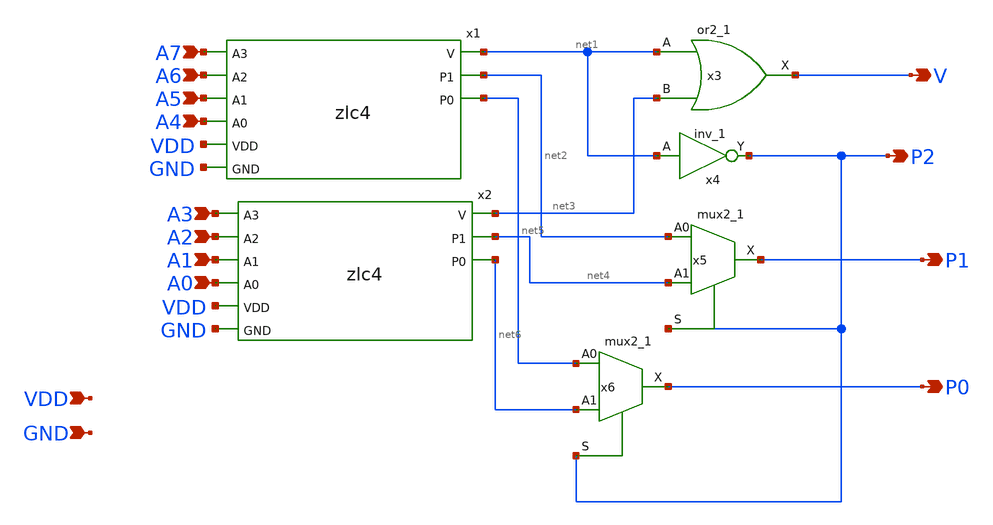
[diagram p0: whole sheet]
** sch_path: xschem/zlc8.sch
**.subckt zlc8 A7 A6 A5 A4 A3 A2 A1 A0 V P2 P1 P0 VDD GND
*.ipin A7
*.ipin A6
*.ipin A5
*.ipin A4
*.ipin A3
*.ipin A2
*.ipin A1
*.ipin A0
*.opin V
*.opin P2
*.opin P1
*.opin P0
*.ipin VDD
*.ipin GND
x3 net1 net3 GND GND VDD VDD V sky130_fd_sc_hd__or2_1
x4 net1 GND GND VDD VDD P2 sky130_fd_sc_hd__inv_1
x5 net2 net4 P2 GND GND VDD VDD P1 sky130_fd_sc_hd__mux2_1
x6 net5 net6 P2 GND GND VDD VDD P0 sky130_fd_sc_hd__mux2_1
x1 A7 net1 A6 net2 A5 A4 net5 VDD GND zlc4
x2 A3 net3 A2 net4 A1 A0 net6 VDD GND zlc4
**.ends

* expanding   symbol:  zlc4.sym # of pins=9
** sym_path: xschem/zlc4.sym
** sch_path: xschem/zlc4.sch
.subckt zlc4 A3 V A2 P1 A1 A0 P0 VDD GND
*.ipin A3
*.ipin A2
*.ipin A1
*.ipin A0
*.opin V
*.opin P1
*.opin P0
*.ipin VDD
*.ipin GND
x3 net1 net2 GND GND VDD VDD V sky130_fd_sc_hd__or2_1
x4 net1 GND GND VDD VDD P1 sky130_fd_sc_hd__inv_1
x5 net3 net4 P1 GND GND VDD VDD P0 sky130_fd_sc_hd__mux2_1
x1 A3 net1 A2 net3 VDD GND zlc2
x2 A1 net2 A0 net4 VDD GND zlc2
.ends


* expanding   symbol:  zlc2.sym # of pins=6
** sym_path: xschem/zlc2.sym
** sch_path: xschem/zlc2.sch
.subckt zlc2 HI V LO P VDD GND
*.ipin HI
*.ipin LO
*.opin V
*.opin P
*.ipin VDD
*.ipin GND
x1 HI LO GND GND VDD VDD V sky130_fd_sc_hd__or2_1
x2 HI GND GND VDD VDD P sky130_fd_sc_hd__inv_1
.ends

.end
